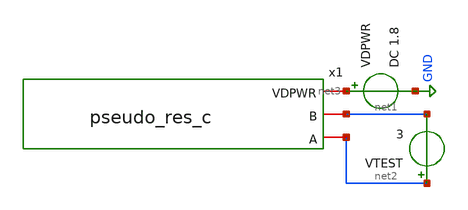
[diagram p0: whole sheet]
** sch_path: xschem/tb_psuedo_res_c.sch
**.subckt tb_psuedo_res_c
x1 net3 net1 net2 pseudo_res_c
VDPWR net3 GND DC 1.8
VTEST net2 net1 3
**** begin user architecture code


.lib /foss/pdks/sky130A/libs.tech/ngspice/sky130.lib.spice tt

.option savecurrents
.temp 27

.control
save all

dc VTEST -0.5 0.5 1m

plot abs(i(vtest))
plot i(vtest)

.endc


**** end user architecture code
**.ends

* expanding   symbol:  pseudo_res_c.sym # of pins=3
** sym_path: xschem/pseudo_res_c.sym
** sch_path: xschem/pseudo_res_c.sch
.subckt pseudo_res_c VDPWR B A
*.iopin A
*.iopin B
*.iopin VDPWR
XP1 A net1 net1 VDPWR sky130_fd_pr__pfet_01v8 L=5 W=0.5 nf=1 ad='int((1 + 1)/2) * 0.5 / 1 * 0.29' as='int((1 + 2)/2) * 0.5 / 1 * 0.29'
+ pd='2*int((1 + 1)/2) * (0.5 / 1 + 0.29)' ps='2*int((1 + 2)/2) * (0.5 / 1 + 0.29)' nrd='0.29 / 0.5 ' nrs='0.29 / 0.5 '
+ sa=0 sb=0 sd=0 mult=10 m=10
XP2 net1 net1 B VDPWR sky130_fd_pr__pfet_01v8 L=5 W=0.5 nf=1 ad='int((1 + 1)/2) * 0.5 / 1 * 0.29' as='int((1 + 2)/2) * 0.5 / 1 * 0.29'
+ pd='2*int((1 + 1)/2) * (0.5 / 1 + 0.29)' ps='2*int((1 + 2)/2) * (0.5 / 1 + 0.29)' nrd='0.29 / 0.5 ' nrs='0.29 / 0.5 '
+ sa=0 sb=0 sd=0 mult=10 m=10
.ends

.GLOBAL GND
.end
